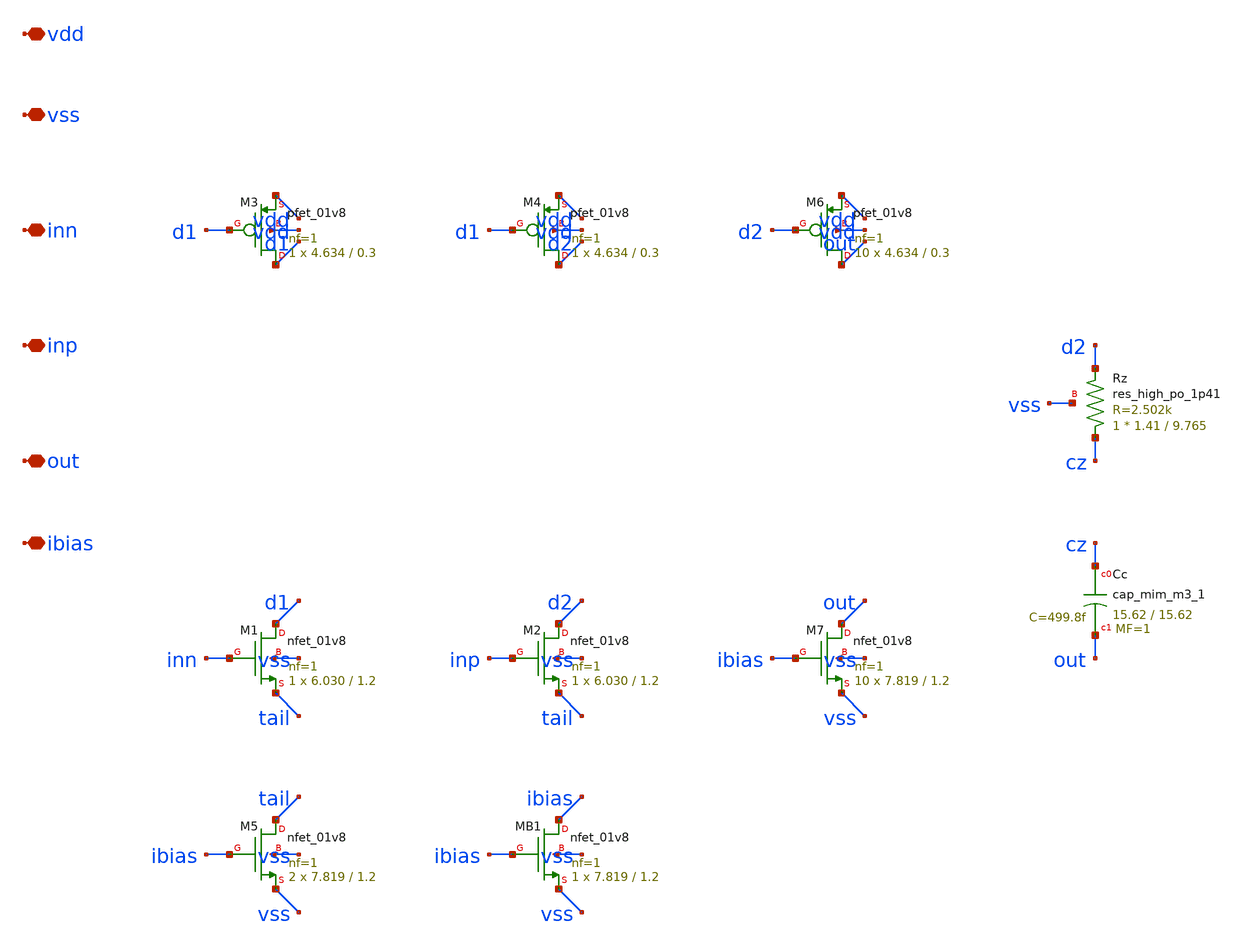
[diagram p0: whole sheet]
** sch_path: design/opamp_core.sch
**.subckt opamp_core vdd vss inn inp out ibias
*.iopin vdd
*.iopin vss
*.iopin inn
*.iopin inp
*.iopin out
*.iopin ibias
XM3 d1 d1 vdd vdd sky130_fd_pr__pfet_01v8 L=0.3 W=4.634 nf=1 ad='int((nf+1)/2) * W/nf * 0.29' as='int((nf+2)/2) * W/nf * 0.29'
+ pd='2*int((nf+1)/2) * (W/nf + 0.29)' ps='2*int((nf+2)/2) * (W/nf + 0.29)' nrd='0.29 / W' nrs='0.29 / W'
+ sa=0 sb=0 sd=0 mult=1 m=1
XM4 d2 d1 vdd vdd sky130_fd_pr__pfet_01v8 L=0.3 W=4.634 nf=1 ad='int((nf+1)/2) * W/nf * 0.29' as='int((nf+2)/2) * W/nf * 0.29'
+ pd='2*int((nf+1)/2) * (W/nf + 0.29)' ps='2*int((nf+2)/2) * (W/nf + 0.29)' nrd='0.29 / W' nrs='0.29 / W'
+ sa=0 sb=0 sd=0 mult=1 m=1
XM1 d1 inn tail vss sky130_fd_pr__nfet_01v8 L=1.2 W=6.030 nf=1 ad='int((1 + 1)/2) * 6.030 / 1 * 0.29'
+ as='int((1 + 2)/2) * 6.030 / 1 * 0.29' pd='2*int((1 + 1)/2) * (6.030 / 1 + 0.29)' ps='2*int((1 + 2)/2) * (6.030 / 1 + 0.29)'
+ nrd='0.29 / 6.030 ' nrs='0.29 / 6.030 ' sa=0 sb=0 sd=0 mult=1 m=1
XM2 d2 inp tail vss sky130_fd_pr__nfet_01v8 L=1.2 W=6.030 nf=1 ad='int((1 + 1)/2) * 6.030 / 1 * 0.29'
+ as='int((1 + 2)/2) * 6.030 / 1 * 0.29' pd='2*int((1 + 1)/2) * (6.030 / 1 + 0.29)' ps='2*int((1 + 2)/2) * (6.030 / 1 + 0.29)'
+ nrd='0.29 / 6.030 ' nrs='0.29 / 6.030 ' sa=0 sb=0 sd=0 mult=1 m=1
XM5 tail ibias vss vss sky130_fd_pr__nfet_01v8 L=1.2 W=7.819 nf=1 ad='int((1 + 1)/2) * 7.819 / 1 * 0.29'
+ as='int((1 + 2)/2) * 7.819 / 1 * 0.29' pd='2*int((1 + 1)/2) * (7.819 / 1 + 0.29)' ps='2*int((1 + 2)/2) * (7.819 / 1 + 0.29)'
+ nrd='0.29 / 7.819 ' nrs='0.29 / 7.819 ' sa=0 sb=0 sd=0 mult=2 m=2
XMB1 ibias ibias vss vss sky130_fd_pr__nfet_01v8 L=1.2 W=7.819 nf=1 ad='int((1 + 1)/2) * 7.819 / 1 * 0.29'
+ as='int((1 + 2)/2) * 7.819 / 1 * 0.29' pd='2*int((1 + 1)/2) * (7.819 / 1 + 0.29)' ps='2*int((1 + 2)/2) * (7.819 / 1 + 0.29)'
+ nrd='0.29 / 7.819 ' nrs='0.29 / 7.819 ' sa=0 sb=0 sd=0 mult=1 m=1
XM6 out d2 vdd vdd sky130_fd_pr__pfet_01v8 L=0.3 W=4.634 nf=1 ad='int((nf+1)/2) * W/nf * 0.29' as='int((nf+2)/2) * W/nf * 0.29'
+ pd='2*int((nf+1)/2) * (W/nf + 0.29)' ps='2*int((nf+2)/2) * (W/nf + 0.29)' nrd='0.29 / W' nrs='0.29 / W'
+ sa=0 sb=0 sd=0 mult=10 m=10
XM7 out ibias vss vss sky130_fd_pr__nfet_01v8 L=1.2 W=7.819 nf=1 ad='int((1 + 1)/2) * 7.819 / 1 * 0.29'
+ as='int((1 + 2)/2) * 7.819 / 1 * 0.29' pd='2*int((1 + 1)/2) * (7.819 / 1 + 0.29)' ps='2*int((1 + 2)/2) * (7.819 / 1 + 0.29)'
+ nrd='0.29 / 7.819 ' nrs='0.29 / 7.819 ' sa=0 sb=0 sd=0 mult=10 m=10
XRz cz d2 vss sky130_fd_pr__res_high_po_1p41 L=9.765 mult=1 m=1
XCc cz out sky130_fd_pr__cap_mim_m3_1 W=15.62 L=15.62 MF=1 m=1
**.ends
.end
